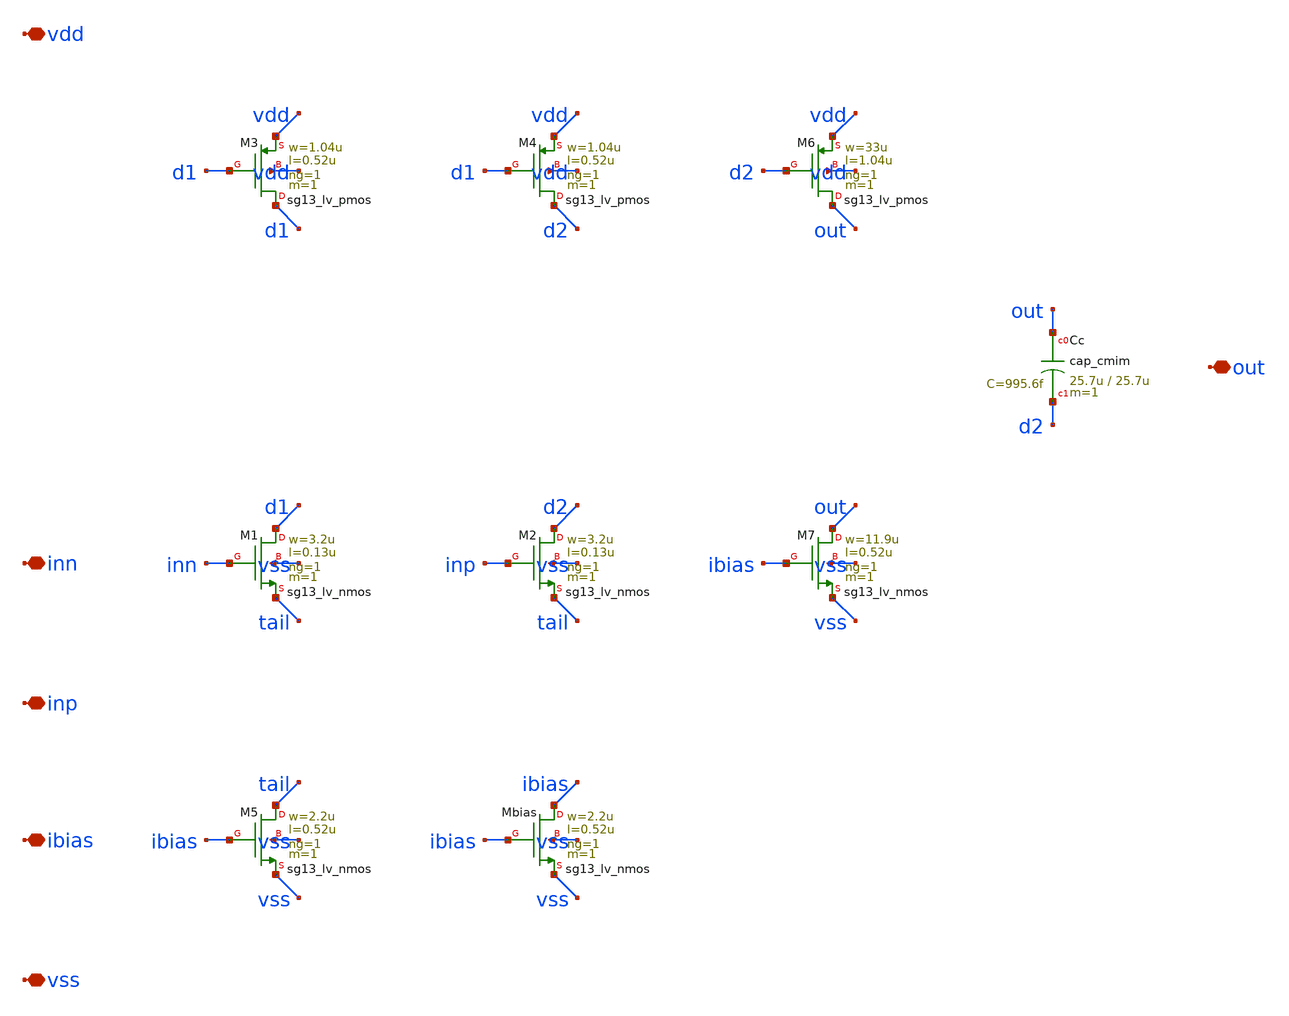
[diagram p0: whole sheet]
** sch_path: design/opamp_core.sch
**.subckt opamp_core vdd vss inn inp out ibias
*.iopin vdd
*.iopin vss
*.iopin inn
*.iopin inp
*.iopin out
*.iopin ibias
XM1 d1 inn tail vss sg13_lv_nmos w=3.2u l=0.13u ng=1 m=1 mm_ok=1
XM2 d2 inp tail vss sg13_lv_nmos w=3.2u l=0.13u ng=1 m=1 mm_ok=1
XM3 d1 d1 vdd vdd sg13_lv_pmos w=1.04u l=0.52u ng=1 m=1 mm_ok=1
XM4 d2 d1 vdd vdd sg13_lv_pmos w=1.04u l=0.52u ng=1 m=1 mm_ok=1
XM5 tail ibias vss vss sg13_lv_nmos w=2.2u l=0.52u ng=1 m=1 mm_ok=1
XMbias ibias ibias vss vss sg13_lv_nmos w=2.2u l=0.52u ng=1 m=1 mm_ok=1
XM6 out d2 vdd vdd sg13_lv_pmos w=33u l=1.04u ng=1 m=1 mm_ok=1
XM7 out ibias vss vss sg13_lv_nmos w=11.9u l=0.52u ng=1 m=1 mm_ok=1
XCc out d2 cap_cmim w=25.7u l=25.7u m=1 mm_ok=1
**.ends
.end
